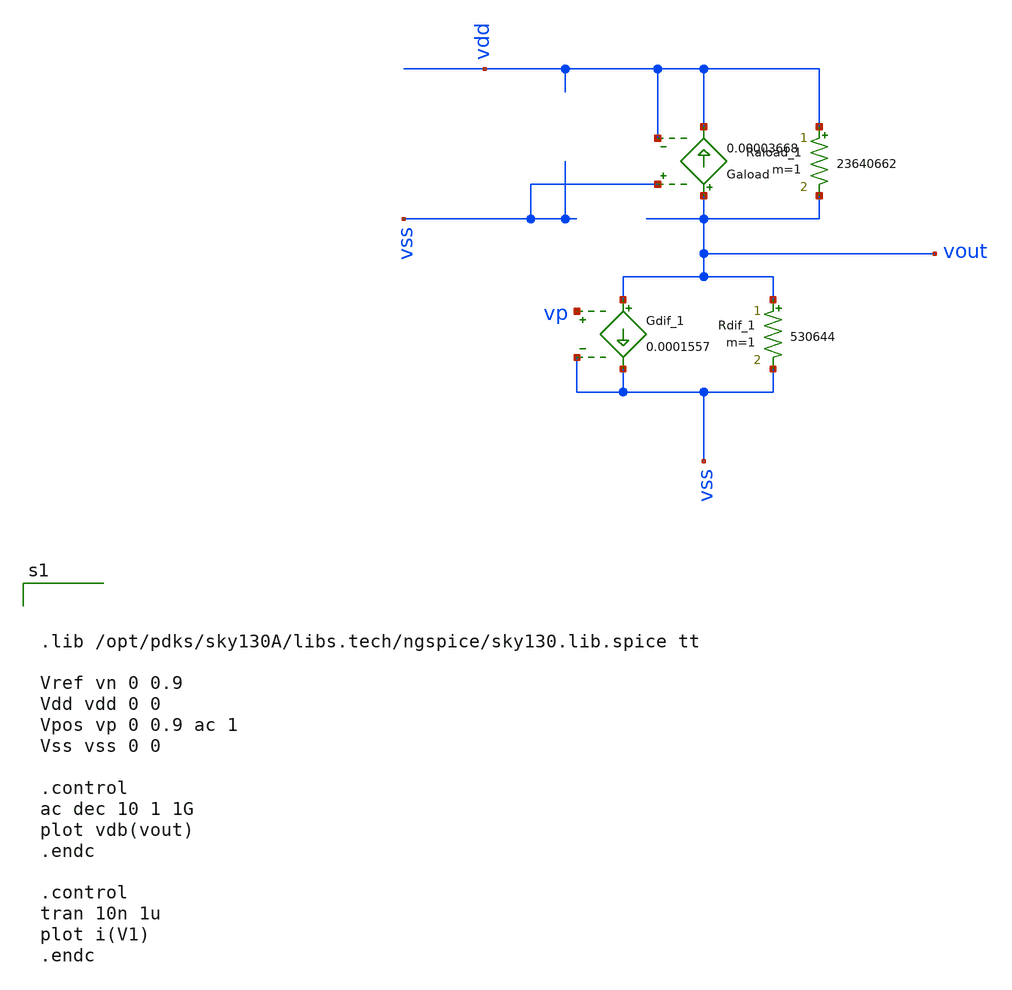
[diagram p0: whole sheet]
** sch_path: test-python/sstadex/xschem/ota_cap_tb.sch
**.subckt ota_cap_tb
Rdif_1 vout vss 530644 m=1
Gdif_1 vout vss vp vss 0.0001557
Raload_1 vdd vout 23640662 m=1
Gaload vout vdd vss vdd 0.00003668
**** begin user architecture code



.lib /opt/pdks/sky130A/libs.tech/ngspice/sky130.lib.spice tt

Vref vn 0 0.9
Vdd vdd 0 0
Vpos vp 0 0.9 ac 1
Vss vss 0 0

.control
ac dec 10 1 1G
plot vdb(vout)
.endc

.control
tran 10n 1u
plot i(V1)
.endc



**** end user architecture code
**.ends
.end
